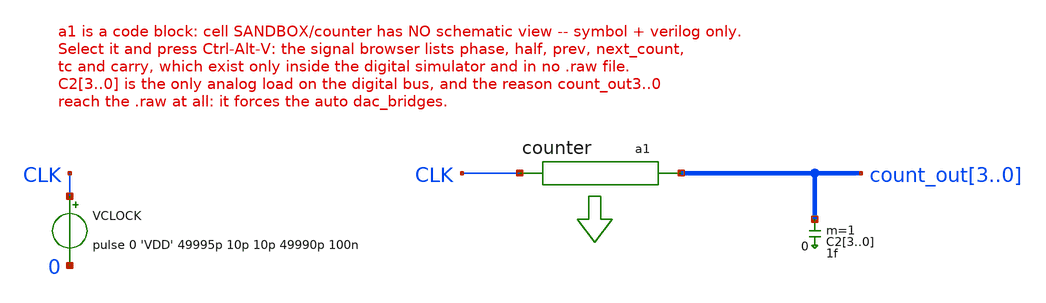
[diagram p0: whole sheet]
** sch_path: xschem_libs_newsym/SANDBOX/tb_counter_wrapper/schematic/tb_counter_wrapper.sch
**.subckt tb_counter_wrapper
VCLOCK CLK 0 pulse 0 'VDD' 49995p 10p 10p 49990p 100n
a1 [ CLK ] [ count_out3 count_out2 count_out1 count_out0 ] counter
C23 count_out3 0 1f m=1
C22 count_out2 0 1f m=1
C21 count_out1 0 1f m=1
C20 count_out0 0 1f m=1
**.ends
**** begin user architecture code
.model counter d_cosim simulation="./counter.so" sim_args=["counter.vcd"] delay=0
**** end user architecture code
.end
